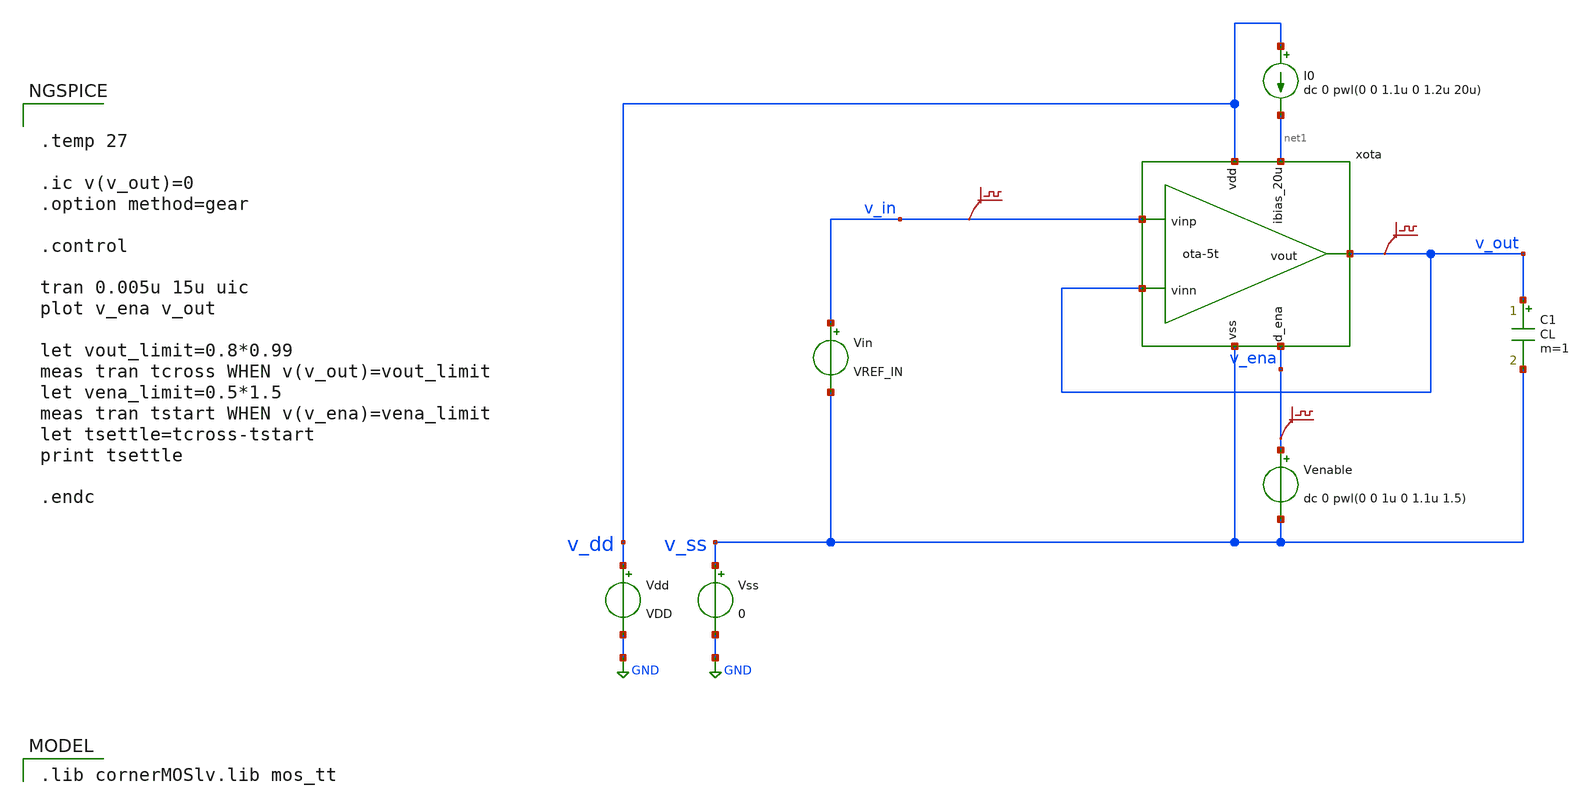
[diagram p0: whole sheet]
** sch_path: platform/examples/OTA/5t-ota/ihp-sg13g2/xschem/ota-5t_tb-tran.sch
* (c) 2024-2025 H. Pretl, Apache-2.0 license
**.subckt ota-5t_tb-tran
Vdd v_dd GND VDD
xota v_dd v_out v_in v_out net1 v_ena v_ss ota-5t
Vss v_ss GND 0
C1 v_out v_ss CL m=1
Vin v_in v_ss VREF_IN
I0 v_dd net1 dc 0 pwl(0 0 1.1u 0 1.2u 20u)
Venable v_ena v_ss dc 0 pwl(0 0 1u 0 1.1u 1.5)
.save v(v_in)
.save v(v_out)
.save v(v_ena)
**** begin user architecture code
 .lib cornerMOSlv.lib mos_tt



.temp 27

.ic v(v_out)=0
.option method=gear

.control

tran 0.005u 15u uic
plot v_ena v_out

let vout_limit=0.8*0.99
meas tran tcross WHEN v(v_out)=vout_limit
let vena_limit=0.5*1.5
meas tran tstart WHEN v(v_ena)=vena_limit
let tsettle=tcross-tstart
print tsettle

.endc





.param VDD=1.5
.param CL=50f
.param VREF_IN=0.8

.param x_dut_nfet_input_w=0.5u
.param x_dut_nfet_input_l=5.0u

.param x_dut_nfet_mirror_w=2.0u
.param x_dut_nfet_mirror_l=5.0u

.param x_dut_pfet_load_w=1.5u
.param x_dut_pfet_load_l=5.0u

.param x_dut_nfet_mirror_ref_w=2.0u
.param x_dut_nfet_mirror_ref_l=5.0u



**** end user architecture code
**.ends

* expanding   symbol:  ota-5t.sym # of pins=7
** sym_path: ota-5t.sym
** sch_path: ota-5t.sch
.subckt ota-5t vdd vout vinp vinn ibias_20u d_ena vss
*.ipin ibias_20u
*.iopin vdd
*.iopin vss
*.ipin vinp
*.ipin vinn
*.opin vout
*.ipin d_ena
XM5 tail gate_n vss vss sg13_lv_nmos w=x_dut_nfet_mirror_w l=x_dut_nfet_mirror_l ng=1 m=1 mm_ok=1
XM4 vout gate_p vdd vdd sg13_lv_pmos w=x_dut_pfet_load_w l=x_dut_pfet_load_l ng=1 m=1 mm_ok=1
XM1 gate_p vinp tail vss sg13_lv_nmos w=x_dut_nfet_input_w l=x_dut_nfet_input_l ng=1 m=1 mm_ok=1
XM2 vout vinn tail vss sg13_lv_nmos w=x_dut_nfet_input_w l=x_dut_nfet_input_l ng=1 m=1 mm_ok=1
XM3 gate_p gate_p vdd vdd sg13_lv_pmos w=x_dut_pfet_load_w l=x_dut_pfet_load_l ng=1 m=1 mm_ok=1
XM6 ibias_20u gate_n vss vss sg13_lv_nmos w=x_dut_nfet_mirror_ref_w l=x_dut_nfet_mirror_ref_l ng=1
+ m=1 mm_ok=1
XM9 gate_n ena_n vss vss sg13_lv_nmos w=0.5u l=0.13u ng=1 m=1 mm_ok=1
XM11 gate_p ena vdd vdd sg13_lv_pmos w=1.5u l=0.13u ng=1 m=1 mm_ok=1
XM7 ena ena_n vss vss sg13_lv_nmos w=0.5u l=0.13u ng=1 m=1 mm_ok=1
XM8 ena ena_n vdd vdd sg13_lv_pmos w=1.5u l=0.13u ng=1 m=1 mm_ok=1
XM10 ibias_20u ena gate_n vss sg13_lv_nmos w=0.5u l=0.13u ng=1 m=1 mm_ok=1
XM12 ena_n d_ena vss vss sg13_lv_nmos w=0.5u l=0.13u ng=1 m=1 mm_ok=1
XM13 ena_n d_ena vdd vdd sg13_lv_pmos w=1.5u l=0.13u ng=1 m=1 mm_ok=1
.ends

.GLOBAL GND
.end
